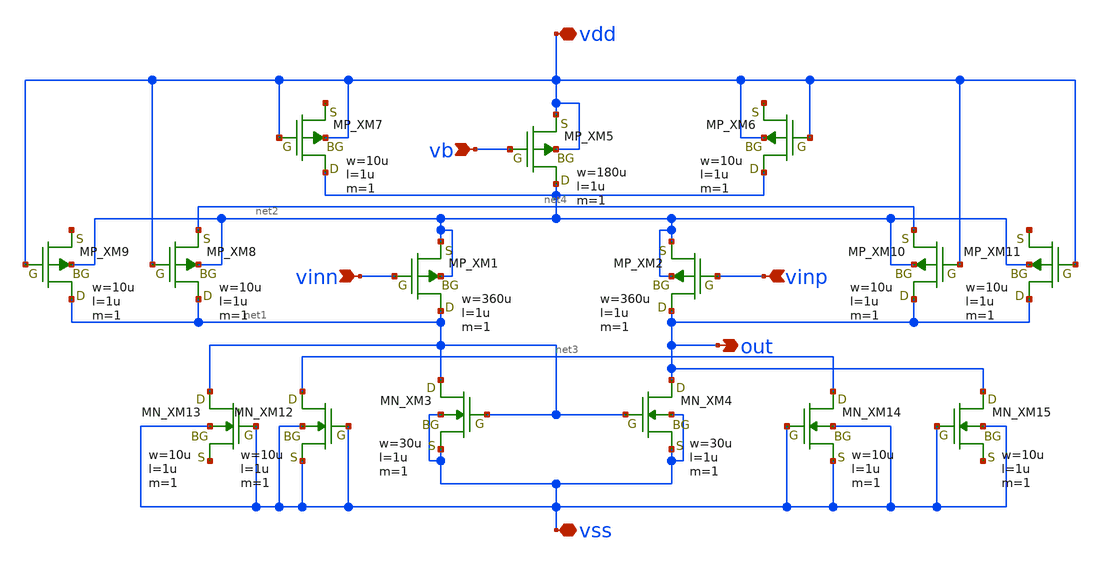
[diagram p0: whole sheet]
** sch_path: TR10/opamp/diff_dp.sch
**.subckt diff_dp vinn vinp vb out vdd vss
*.ipin vinn
*.ipin vinp
*.ipin vb
*.opin out
*.iopin vdd
*.iopin vss
XM5 net2 vb vdd vdd PMOS w=180u l=1u as=0 ad=0 ps=0 pd=0 nrd=0 nrs=0 m=1
XM1 net1 vinn net2 net2 PMOS w=360u l=1u as=0 ad=0 ps=0 pd=0 nrd=0 nrs=0 m=1
XM2 out vinp net2 net2 PMOS w=360u l=1u as=0 ad=0 ps=0 pd=0 nrd=0 nrs=0 m=1
XM3 net1 net1 vss vss NMOS w=30u l=1u as=0 ad=0 ps=0 pd=0 nrd=0 nrs=0 m=1
XM4 out net1 vss vss NMOS w=30u l=1u as=0 ad=0 ps=0 pd=0 nrd=0 nrs=0 m=1
XM6 net2 vdd net5 vdd PMOS w=10u l=1u as=0 ad=0 ps=0 pd=0 nrd=0 nrs=0 m=1
XM7 net2 vdd net6 vdd PMOS w=10u l=1u as=0 ad=0 ps=0 pd=0 nrd=0 nrs=0 m=1
XM8 net1 vdd net4 net2 PMOS w=10u l=1u as=0 ad=0 ps=0 pd=0 nrd=0 nrs=0 m=1
XM9 net1 vdd net7 net2 PMOS w=10u l=1u as=0 ad=0 ps=0 pd=0 nrd=0 nrs=0 m=1
XM10 out vdd net4 net2 PMOS w=10u l=1u as=0 ad=0 ps=0 pd=0 nrd=0 nrs=0 m=1
XM11 out vdd net8 net2 PMOS w=10u l=1u as=0 ad=0 ps=0 pd=0 nrd=0 nrs=0 m=1
XM12 net3 vss vss vss NMOS w=10u l=1u as=0 ad=0 ps=0 pd=0 nrd=0 nrs=0 m=1
XM13 net1 vss net9 vss NMOS w=10u l=1u as=0 ad=0 ps=0 pd=0 nrd=0 nrs=0 m=1
XM14 net3 vss vss vss NMOS w=10u l=1u as=0 ad=0 ps=0 pd=0 nrd=0 nrs=0 m=1
XM15 out vss net10 vss NMOS w=10u l=1u as=0 ad=0 ps=0 pd=0 nrd=0 nrs=0 m=1
**.ends
.end
